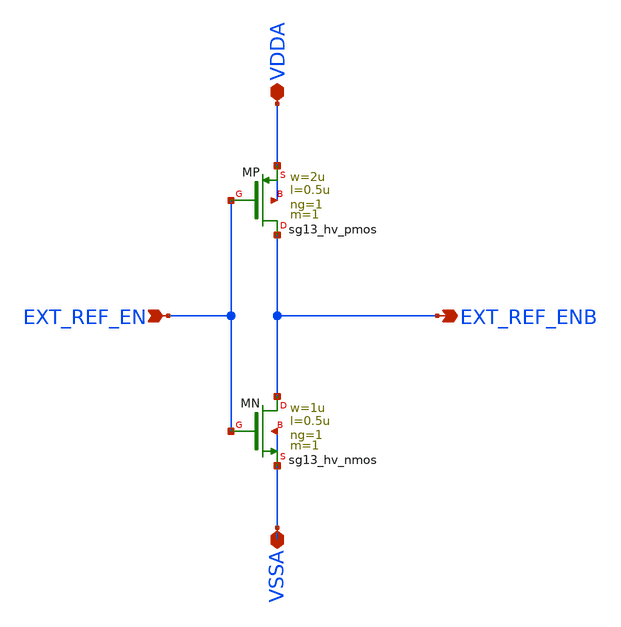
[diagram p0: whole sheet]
** sch_path: EXT_REF_ENB.sch
**.subckt EXT_REF_ENB EXT_REF_EN EXT_REF_ENB VDDA VSSA
*.ipin EXT_REF_EN
*.opin EXT_REF_ENB
*.iopin VDDA
*.iopin VSSA
XMP EXT_REF_ENB EXT_REF_EN VDDA VDDA sg13_hv_pmos w=2u l=0.5u ng=1 m=1 mm_ok=1
XMN EXT_REF_ENB EXT_REF_EN VSSA VSSA sg13_hv_nmos w=1u l=0.5u ng=1 m=1 mm_ok=1
**.ends
.end
